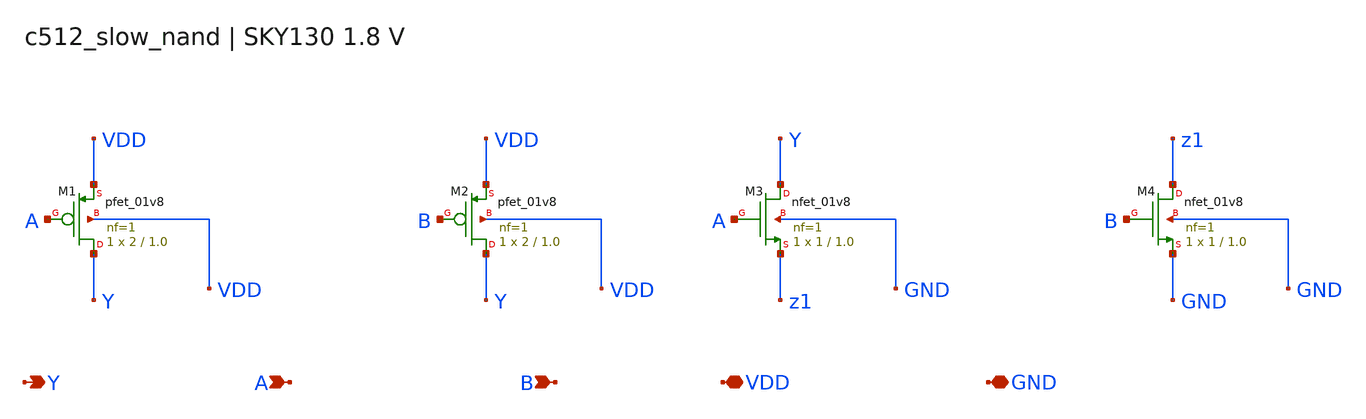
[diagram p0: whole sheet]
** sch_path: c512_slow_nand.sch
**.subckt c512_slow_nand Y A B VDD GND
*.opin Y
*.ipin A
*.ipin B
*.iopin VDD
*.iopin GND
XM1 Y A VDD VDD sky130_fd_pr__pfet_01v8 L=1.0 W=2 nf=1 ad=0.58 as=0.58 pd=4.58 ps=4.58 nrd=0.145
+ nrs=0.145 sa=0 sb=0 sd=0 mult=1 m=1
XM2 Y B VDD VDD sky130_fd_pr__pfet_01v8 L=1.0 W=2 nf=1 ad=0.58 as=0.58 pd=4.58 ps=4.58 nrd=0.145
+ nrs=0.145 sa=0 sb=0 sd=0 mult=1 m=1
XM3 Y A z1 GND sky130_fd_pr__nfet_01v8 L=1.0 W=1 nf=1 ad=0.29 as=0.29 pd=2.58 ps=2.58 nrd=0.29
+ nrs=0.29 sa=0 sb=0 sd=0 mult=1 m=1
XM4 z1 B GND GND sky130_fd_pr__nfet_01v8 L=1.0 W=1 nf=1 ad=0.29 as=0.29 pd=2.58 ps=2.58 nrd=0.29
+ nrs=0.29 sa=0 sb=0 sd=0 mult=1 m=1
**.ends
.end
